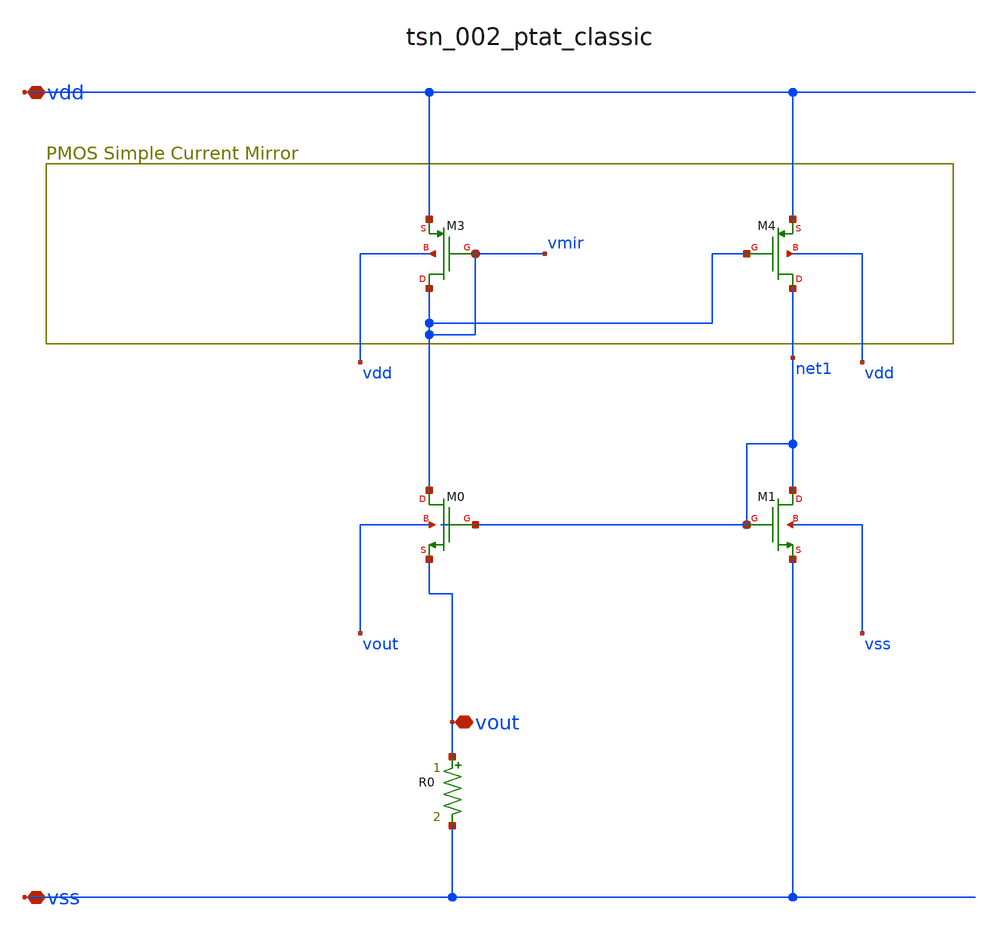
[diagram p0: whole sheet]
** sch_path: analog-db/raw/tsn_002_ptat_classic/tsn_002_ptat_classic_annotated.sch
**.subckt tsn_002_ptat_classic_annotated vdd vout vss
*.iopin vdd
*.iopin vout
*.iopin vss
R0 vout vss x_r0 m=1
XM0 vmir net1 vout vout sg13_lv_nmos w=x_dut_xm0_w l=x_dut_xm0_l ng=1 m=x_dut_xm0_m
XM1 net1 net1 vss vss sg13_lv_nmos w=x_dut_xm1_w l=x_dut_xm1_l ng=1 m=x_dut_xm1_m
XM3 vmir vmir vdd vdd sg13_lv_pmos w=x_dut_xm3_w l=x_dut_xm3_l ng=1 m=x_dut_xm3_m
XM4 net1 vmir vdd vdd sg13_lv_pmos w=x_dut_xm4_w l=x_dut_xm4_l ng=1 m=x_dut_xm4_m
**.ends
.end
